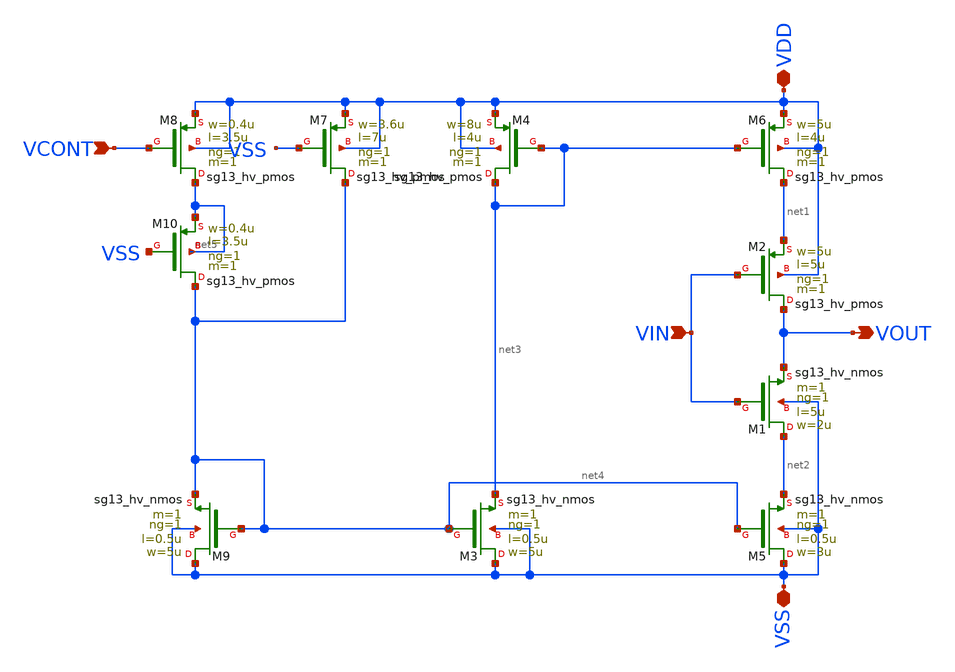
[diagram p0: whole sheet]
** sch_path: xschem/stage_v6p5_IHP.sch
**.subckt stage_v6p5_IHP VIN VOUT VDD VSS VCONT
*.ipin VIN
*.opin VOUT
*.iopin VDD
*.iopin VSS
*.ipin VCONT
XM9 VSS net4 net4 VSS sg13_hv_nmos w=5u l=0.5u ng=1 m=1 mm_ok=1
XM3 VSS net4 net3 VSS sg13_hv_nmos w=5u l=0.5u ng=1 m=1 mm_ok=1
XM5 VSS net4 net2 VSS sg13_hv_nmos w=3u l=0.5u ng=1 m=1 mm_ok=1
XM8 net5 VCONT VDD VDD sg13_hv_pmos w=0.4u l=3.5u ng=1 m=1 mm_ok=1
XM4 net3 net3 VDD VDD sg13_hv_pmos w=8u l=4u ng=1 m=1 mm_ok=1
XM6 net1 net3 VDD VDD sg13_hv_pmos w=5u l=4u ng=1 m=1 mm_ok=1
XM2 VOUT VIN net1 VDD sg13_hv_pmos w=5u l=5u ng=1 m=1 mm_ok=1
XM1 net2 VIN VOUT VSS sg13_hv_nmos w=2u l=5u ng=1 m=1 mm_ok=1
XM7 net4 VSS VDD VDD sg13_hv_pmos w=3.6u l=7u ng=1 m=1 mm_ok=1
XM10 net4 VSS net5 net5 sg13_hv_pmos w=0.4u l=3.5u ng=1 m=1 mm_ok=1
**.ends
.end
